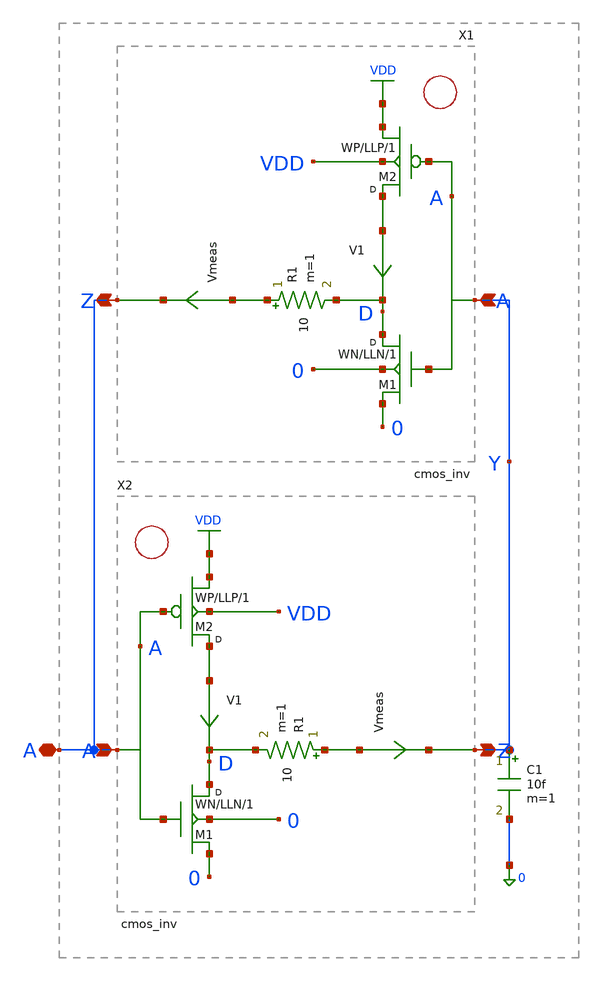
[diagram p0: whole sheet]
** sch_path: xschem-src/xschem_library/examples/bus_keeper.sch
* Copyright (C) 1998-2026 Stefan Frederik Schippers
* This program is free software; you can redistribute it and/or modify
* it under the terms of the GNU General Public License as published by
* the Free Software Foundation; either version 2 of the License, or
* (at your option) any later version.
* This program is distributed in the hope that it will be useful,
* but WITHOUT ANY WARRANTY; without even the implied warranty of
* MERCHANTABILITY or FITNESS FOR A PARTICULAR PURPOSE.  See the
* GNU General Public License for more details.
* You should have received a copy of the GNU General Public License
* along with this program; if not, write to the Free Software
**.subckt bus_keeper A
*.iopin A
X2 Y A cmos_inv WN=15u WP=45u LLN=3u LLP=3u m=1
X1 A Y cmos_inv WN=WN_FB WP=WP_FB LLN=3u LLP=3u m=1
C1 Y 0 10f m=1
**.ends

* expanding   symbol:  cmos_inv.sch # of pins=2
** sym_path: xschem-src/xschem_library/examples/cmos_inv.sch
** sch_path: xschem-src/xschem_library/examples/cmos_inv.sch
.subckt cmos_inv Z A  WN=15u WP=45u LLN=3u LLP=3u
*.opin Z
*.ipin A
M2 net1 A VDD VDD p w=WP l=LLP m=1
M1 D A 0 0 n w=WN l=LLN m=1
R1 net2 D 10 m=1
V1 net1 D 0
.save i(v1)
Vmeas net2 Z 0
.save i(vmeas)
.ends

.GLOBAL VDD
.end
